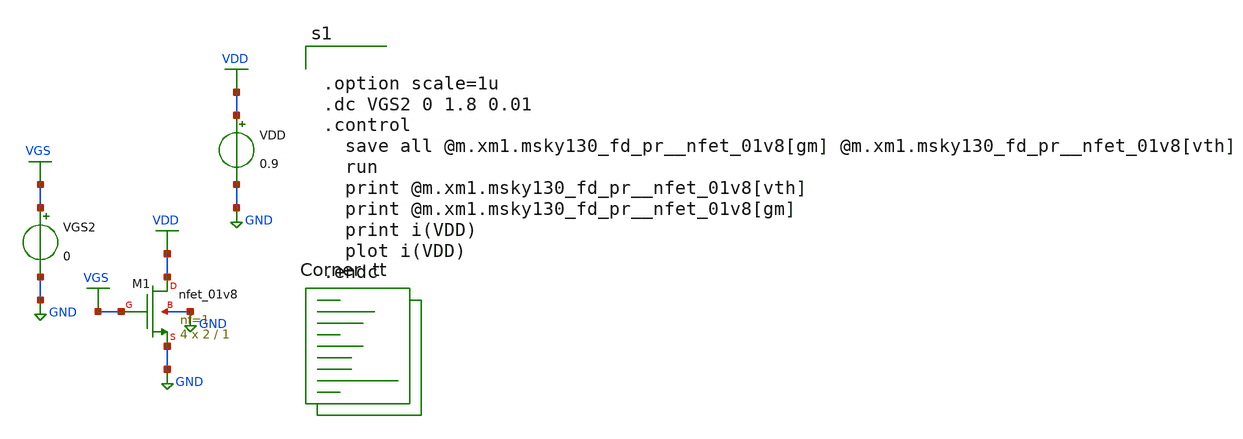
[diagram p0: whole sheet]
** sch_path: analog/schematics/bootcamp_opamp.sch
**.subckt bootcamp_opamp
XM1 VDD VGS GND GND sky130_fd_pr__nfet_01v8 L=1 W=2 nf=1 ad='int((nf+1)/2) * W/nf * 0.29' as='int((nf+2)/2) * W/nf * 0.29'
+ pd='2*int((nf+1)/2) * (W/nf + 0.29)' ps='2*int((nf+2)/2) * (W/nf + 0.29)' nrd='0.29 / W' nrs='0.29 / W'
+ sa=0 sb=0 sd=0 mult=4 m=4
VDD VDD GND 0.9
.save i(vdd)
VGS2 VGS GND 0
**** begin user architecture code


.option scale=1u
.dc VGS2 0 1.8 0.01
.control
  save all @m.xm1.msky130_fd_pr__nfet_01v8[gm] @m.xm1.msky130_fd_pr__nfet_01v8[vth]
  run
  print @m.xm1.msky130_fd_pr__nfet_01v8[vth]
  print @m.xm1.msky130_fd_pr__nfet_01v8[gm]
  print i(VDD)
  plot i(VDD)
.endc


.lib $::SKYWATER_MODELS/sky130.lib.spice tt
**** end user architecture code
**.ends
.GLOBAL GND
.GLOBAL VDD
.GLOBAL VGS
.end
